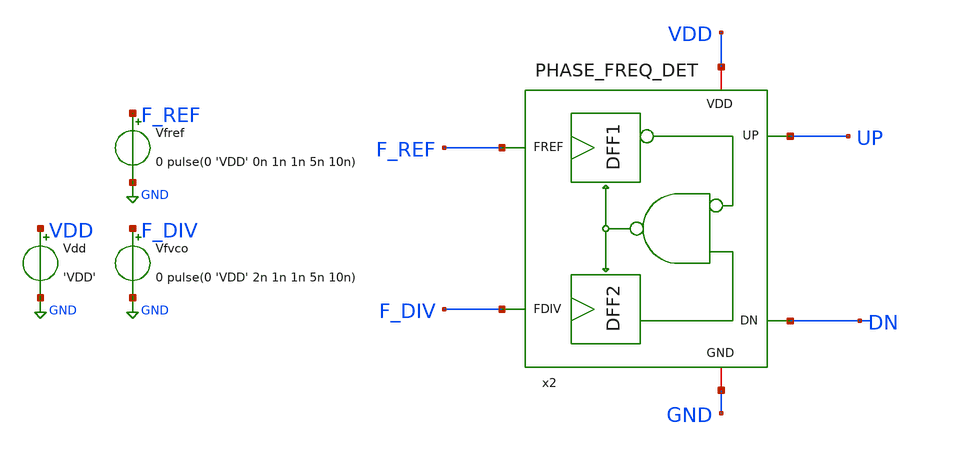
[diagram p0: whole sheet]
** sch_path: xschem/phase-freq-detector/tb_PHASE_FREQ_DET.sch
**.subckt tb_PHASE_FREQ_DET
Vdd VDD GND 'VDD'
Vfvco F_DIV GND 0 pulse(0 'VDD' 2n 1n 1n 5n 10n)
Vfref F_REF GND 0 pulse(0 'VDD' 0n 1n 1n 5n 10n)
x2 F_REF UP VDD GND F_DIV DN PHASE_FREQ_DET
**** begin user architecture code



* Nominal conditions (27 C, 1.2 V). For the Monte Carlo spread of temperature and supply
* used in the paper, replace them by:
*   .param RAW_TEMP = agauss(40, 30, 1)
*   .param TEMPGAUSS = max(20, min(RAW_TEMP, 80))
*   .option temp = 'TEMPGAUSS'
*   .param VDDGAUSS = agauss(1.2, 0.05, 1)
*   .param VDD = 'VDDGAUSS'
.option temp = 27

.param VDD = 1.2
* analysis

.tran 100p 30n uic

.control
run
write tb_PHASE_FREQ_DET.raw
meas tran up_avg avg v(UP) from=10n to=30n
meas tran dn_avg avg v(DN) from=10n to=30n
meas tran up_r2 when v(UP)=0.6 rise=2
meas tran up_f2 when v(UP)=0.6 fall=2
meas tran dn_r2 when v(DN)=0.6 rise=2
meas tran dn_f2 when v(DN)=0.6 fall=2
* supply current (negative = drawn from the source), power = 1.2 V x |idd|
meas tran idd avg i(Vdd) from=10n to=30n
plot v(F_REF) v(F_DIV)
plot v(UP) v(DN)
.endc






.lib cornerMOSlv.lib mos_tt
.lib cornerMOShv.lib mos_tt
.lib cornerHBT.lib hbt_typ
.lib cornerRES.lib res_typ
.include /foss/pdks/ihp-sg13g2/libs.ref/sg13g2_stdcell/spice/sg13g2_stdcell.spice
.global VDD GND




**** end user architecture code
**.ends

* expanding   symbol:  xschem/phase-freq-detector/PHASE_FREQ_DET.sym # of pins=6
** sym_path: xschem/phase-freq-detector/PHASE_FREQ_DET.sym
** sch_path: xschem/phase-freq-detector/PHASE_FREQ_DET.sch
.subckt PHASE_FREQ_DET FREF UP VDD GND FDIV DN
*.opin UP
*.ipin FREF
*.iopin VDD
*.iopin GND
*.opin DN
*.ipin FDIV
* noconn #net2
x1 net1 UP FREF VDD nRST VDD GND sg13g2_dfrbp_2
x2 DN net2 FDIV VDD nRST VDD GND sg13g2_dfrbp_2
x3 nRST net1 DN VDD GND sg13g2_nand2_2
.ends

.GLOBAL GND
.GLOBAL VDD
.end
